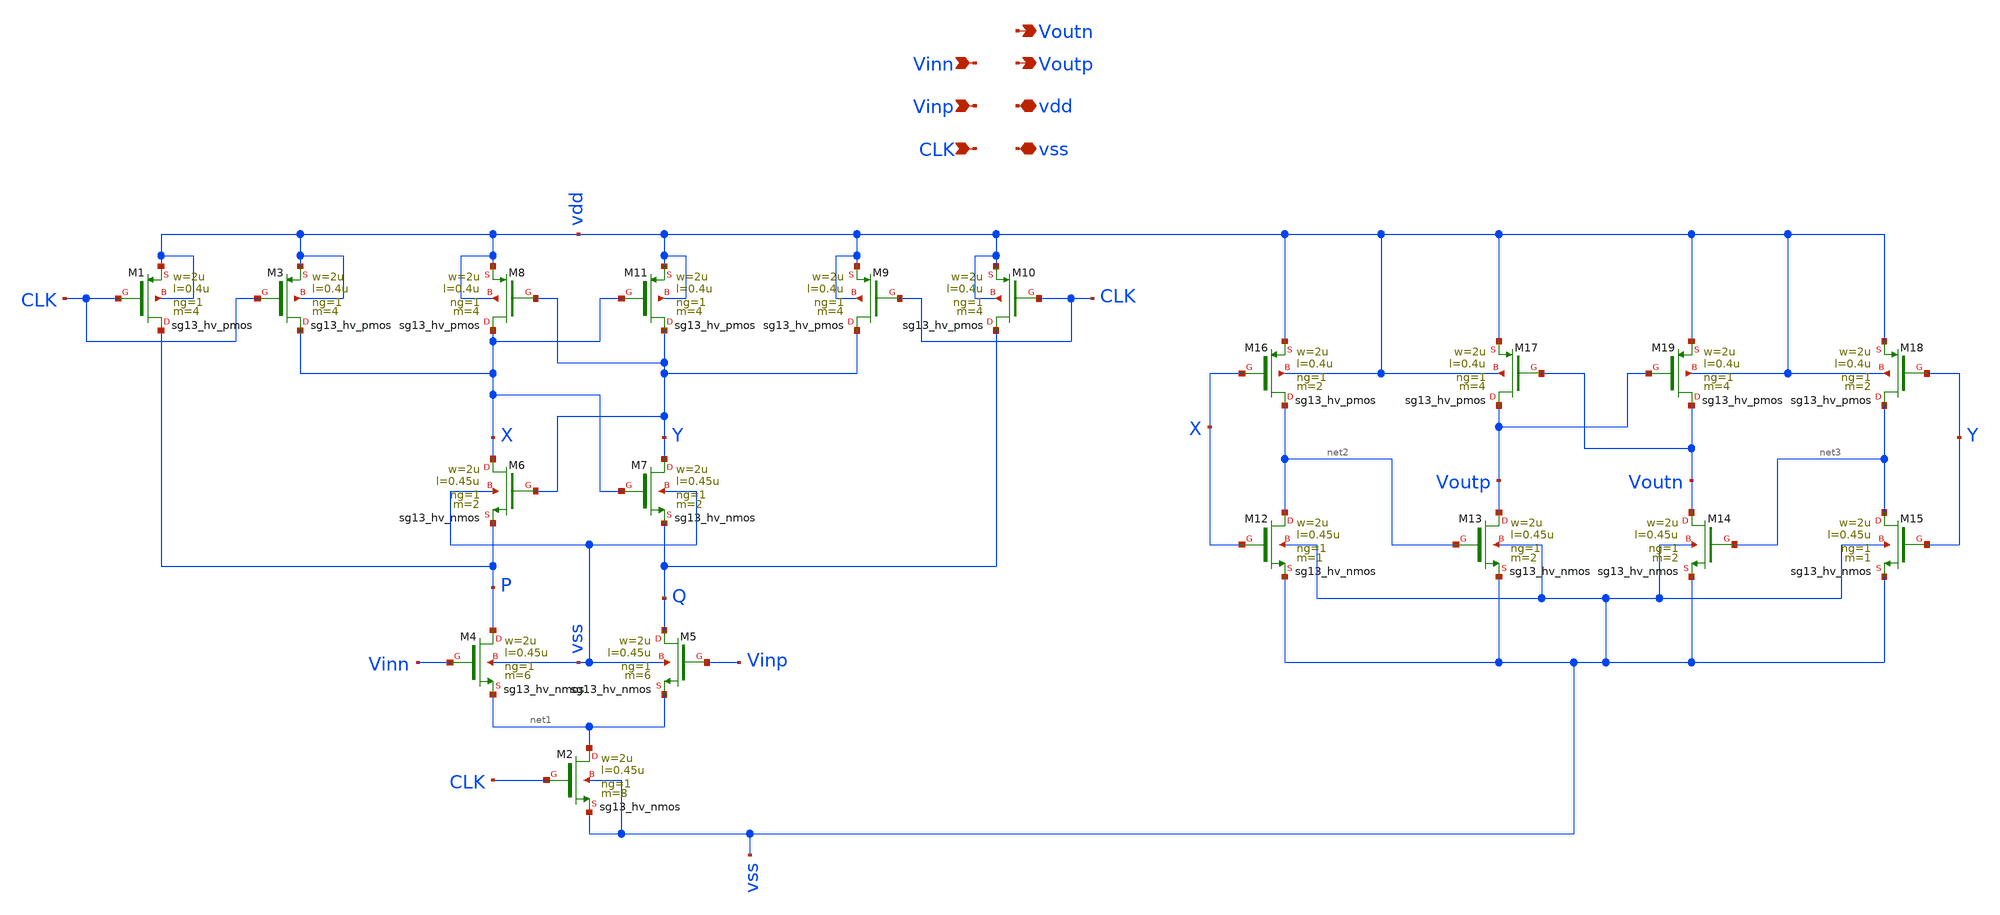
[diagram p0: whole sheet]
** sch_path: circuit_files/sar_adc_test/xschem/strong_arm_comp.sch
**.subckt strong_arm_comp Vinn Voutp vdd Vinp CLK vss Voutn
*.ipin Vinn
*.opin Voutp
*.iopin vdd
*.ipin Vinp
*.ipin CLK
*.iopin vss
*.opin Voutn
XM1 P CLK vdd vdd sg13_hv_pmos w=2u l=0.4u ng=1 m=4 mm_ok=1
XM2 net1 CLK vss vss sg13_hv_nmos w=2u l=0.45u ng=1 m=8 mm_ok=1
XM3 X CLK vdd vdd sg13_hv_pmos w=2u l=0.4u ng=1 m=4 mm_ok=1
XM4 P Vinn net1 vss sg13_hv_nmos w=2u l=0.45u ng=1 m=6 mm_ok=1
XM5 Q Vinp net1 vss sg13_hv_nmos w=2u l=0.45u ng=1 m=6 mm_ok=1
XM6 X Y P vss sg13_hv_nmos w=2u l=0.45u ng=1 m=2 mm_ok=1
XM7 Y X Q vss sg13_hv_nmos w=2u l=0.45u ng=1 m=2 mm_ok=1
XM8 X Y vdd vdd sg13_hv_pmos w=2u l=0.4u ng=1 m=4 mm_ok=1
XM9 Y CLK vdd vdd sg13_hv_pmos w=2u l=0.4u ng=1 m=4 mm_ok=1
XM10 Q CLK vdd vdd sg13_hv_pmos w=2u l=0.4u ng=1 m=4 mm_ok=1
XM11 Y X vdd vdd sg13_hv_pmos w=2u l=0.4u ng=1 m=4 mm_ok=1
XM12 net2 X vss vss sg13_hv_nmos w=2u l=0.45u ng=1 m=1 mm_ok=1
XM13 Voutp net2 vss vss sg13_hv_nmos w=2u l=0.45u ng=1 m=2 mm_ok=1
XM14 Voutn net3 vss vss sg13_hv_nmos w=2u l=0.45u ng=1 m=2 mm_ok=1
XM15 net3 Y vss vss sg13_hv_nmos w=2u l=0.45u ng=1 m=1 mm_ok=1
XM16 net2 X vdd vdd sg13_hv_pmos w=2u l=0.4u ng=1 m=2 mm_ok=1
XM17 Voutp Voutn vdd vdd sg13_hv_pmos w=2u l=0.4u ng=1 m=4 mm_ok=1
XM18 net3 Y vdd vdd sg13_hv_pmos w=2u l=0.4u ng=1 m=2 mm_ok=1
XM19 Voutn Voutp vdd vdd sg13_hv_pmos w=2u l=0.4u ng=1 m=4 mm_ok=1
**.ends
.end
